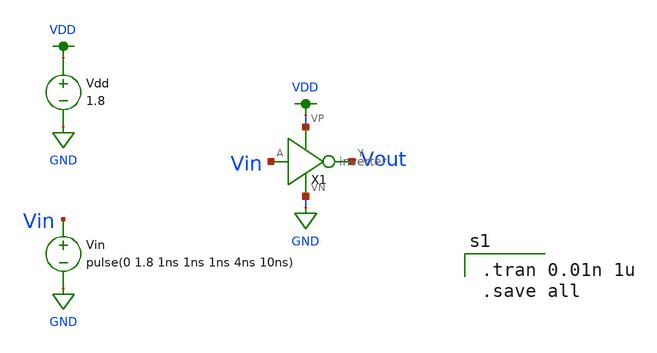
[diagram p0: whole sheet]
** sch_path: MP2/xschem/archive/inverter_tran.sch
**.subckt inverter_tran
Vdd VDD GND 1.8
Vin Vin GND pulse(0 1.8 1ns 1ns 1ns 4ns 10ns)
X1 Vin Vout VDD GND inverter
**** begin user architecture code

.option wnflag=1
.lib ~/skywater/skywater-pdk/libraries/sky130_fd_pr_ngspice/latest/models/sky130.lib.spice tt


.tran 0.01n 1u
.save all

**** end user architecture code
**.ends
.GLOBAL VDD
.GLOBAL GND
.end
